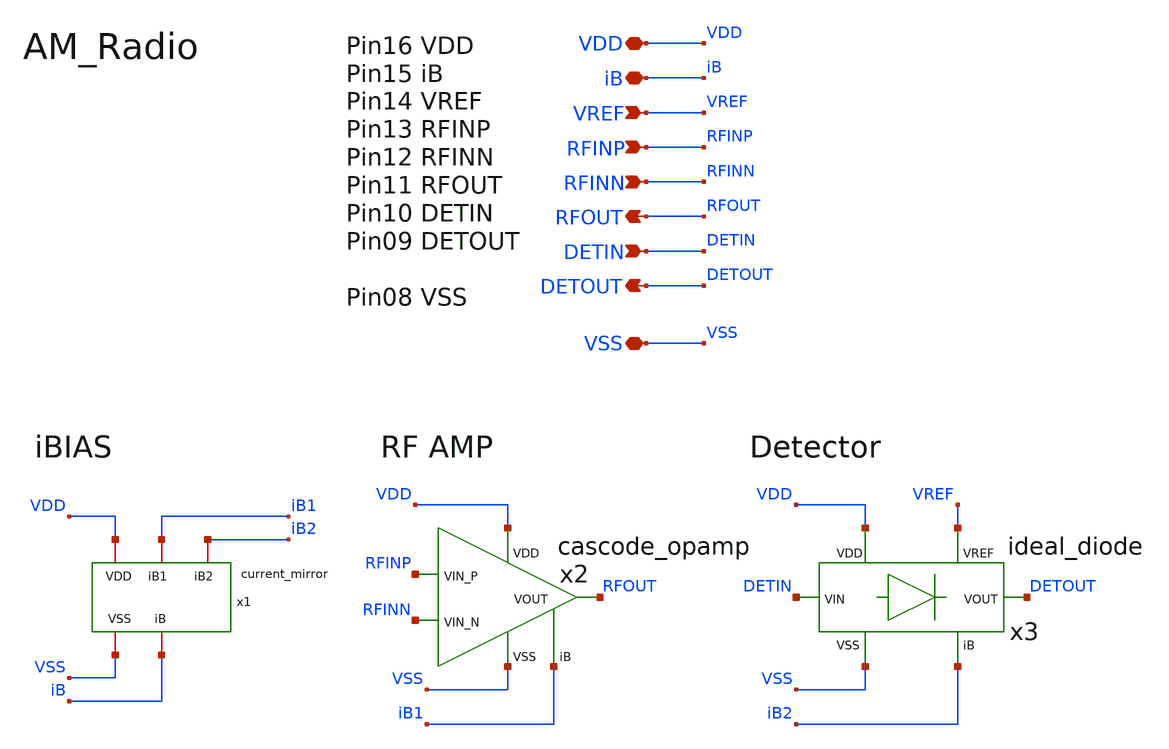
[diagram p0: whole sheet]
** sch_path: member_project/AM_Radio/Yamada3/xschem/AM_Radio.sch
**.subckt AM_Radio VREF VSS VDD iB RFINN RFINP DETIN RFOUT DETOUT
*.ipin VREF
*.iopin VSS
*.iopin VDD
*.iopin iB
*.ipin RFINN
*.ipin RFINP
*.ipin DETIN
*.opin RFOUT
*.opin DETOUT
x3 VDD VSS DETIN DETOUT iB2 VREF ideal_diode
x1 VDD VSS iB iB1 iB2 current_mirror
x2 VDD VSS RFINP RFINN RFOUT iB1 cascode_opamp
**.ends
.end
